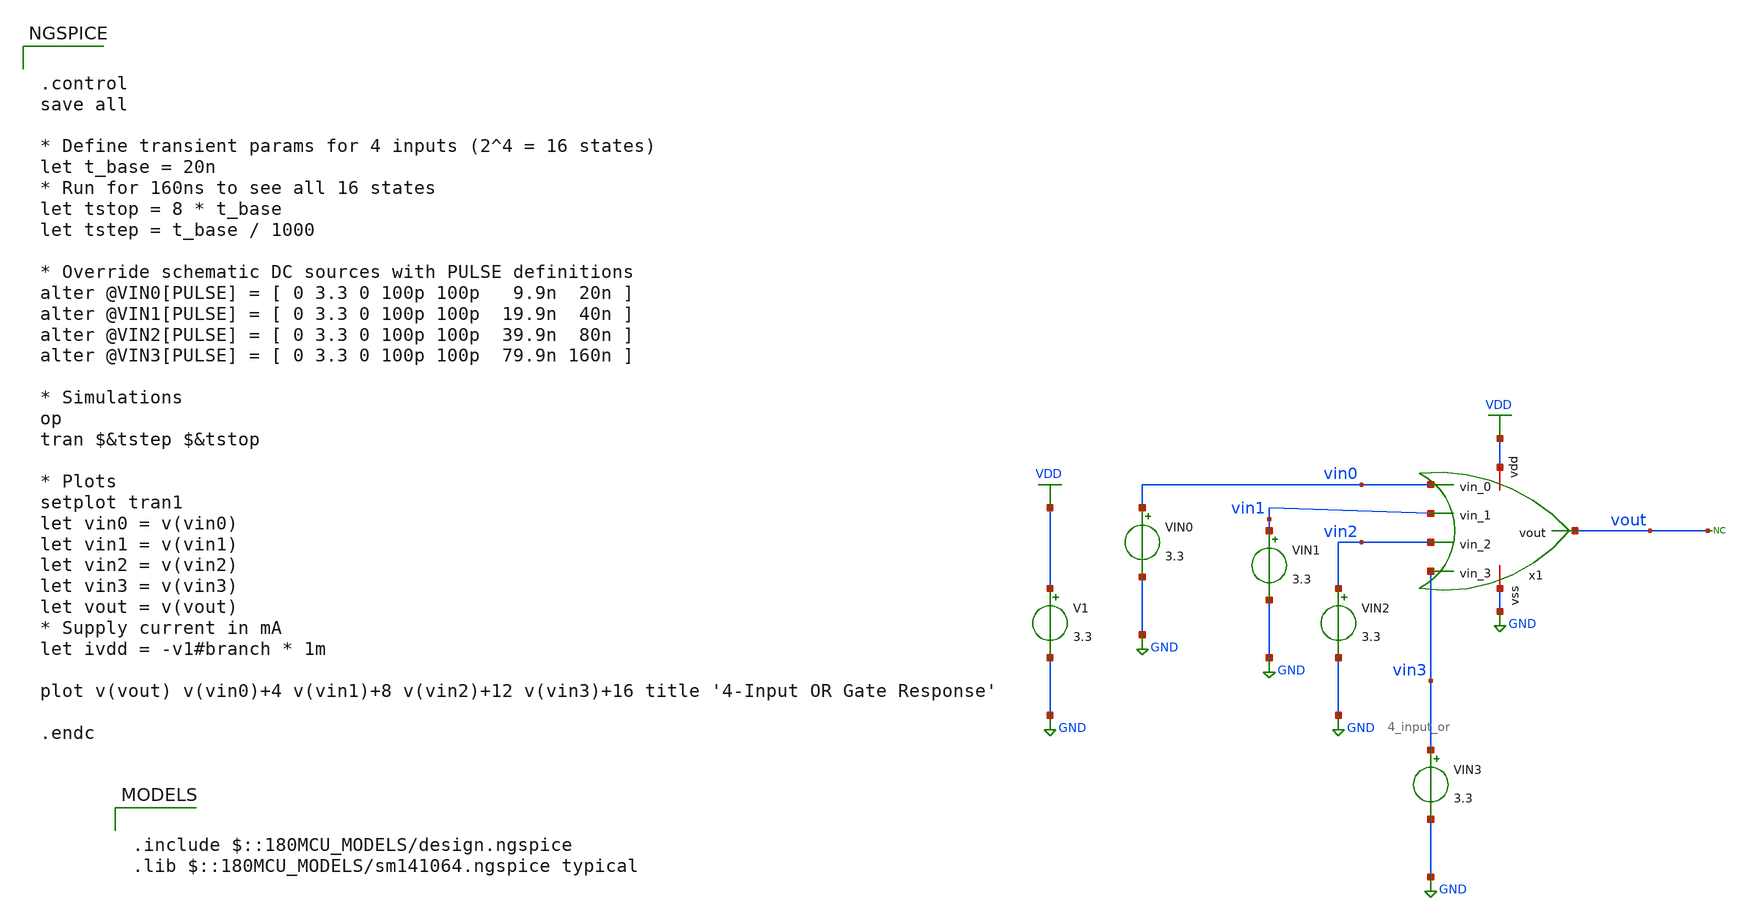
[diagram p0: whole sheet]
** sch_path: designs/4_input_or_tb.sch
**.subckt 4_input_or_tb
V1 VDD GND 3.3
VIN0 vin0 GND 3.3
* noconn vout
VIN2 vin2 GND 3.3
VIN1 vin1 GND 3.3
x1 VDD vin0 vin1 vin2 vin3 vout GND 4_input_or
VIN3 vin3 GND 3.3
**** begin user architecture code

.include $::180MCU_MODELS/design.ngspice
.lib $::180MCU_MODELS/sm141064.ngspice typical



.control
save all

* Define transient params for 4 inputs (2^4 = 16 states)
let t_base = 20n
* Run for 160ns to see all 16 states
let tstop = 8 * t_base
let tstep = t_base / 1000

* Override schematic DC sources with PULSE definitions
alter @VIN0[PULSE] = [ 0 3.3 0 100p 100p   9.9n  20n ]
alter @VIN1[PULSE] = [ 0 3.3 0 100p 100p  19.9n  40n ]
alter @VIN2[PULSE] = [ 0 3.3 0 100p 100p  39.9n  80n ]
alter @VIN3[PULSE] = [ 0 3.3 0 100p 100p  79.9n 160n ]

* Simulations
op
tran $&tstep $&tstop

* Plots
setplot tran1
let vin0 = v(vin0)
let vin1 = v(vin1)
let vin2 = v(vin2)
let vin3 = v(vin3)
let vout = v(vout)
* Supply current in mA
let ivdd = -v1#branch * 1m

plot v(vout) v(vin0)+4 v(vin1)+8 v(vin2)+12 v(vin3)+16 title '4-Input OR Gate Response'

.endc


**** end user architecture code
**.ends

* expanding   symbol:  4_input_or.sym # of pins=7
** sym_path: designs/4_input_or.sym
** sch_path: designs/4_input_or.sch
.subckt 4_input_or vdd vin_0 vin_1 vin_2 vin_3 vout vss
*.iopin vdd
*.iopin vss
*.ipin vin_0
*.ipin vin_1
*.ipin vin_2
*.ipin vin_3
*.opin vout
XM1 net1 vin_0 vdd vdd pfet_03v3 L=0.28u W=0.22u nf=1 ad='int((nf+1)/2) * W/nf * 0.18u' as='int((nf+2)/2) * W/nf * 0.18u'
+ pd='2*int((nf+1)/2) * (W/nf + 0.18u)' ps='2*int((nf+2)/2) * (W/nf + 0.18u)' nrd='0.18u / W' nrs='0.18u / W'
+ sa=0 sb=0 sd=0 m=1
XM2 net4 vin_3 vss vss nfet_03v3 L=0.28u W=0.22u nf=1 ad='int((nf+1)/2) * W/nf * 0.18u' as='int((nf+2)/2) * W/nf * 0.18u'
+ pd='2*int((nf+1)/2) * (W/nf + 0.18u)' ps='2*int((nf+2)/2) * (W/nf + 0.18u)' nrd='0.18u / W' nrs='0.18u / W'
+ sa=0 sb=0 sd=0 m=1
XM3 net2 vin_1 net1 vdd pfet_03v3 L=0.28u W=0.22u nf=1 ad='int((nf+1)/2) * W/nf * 0.18u' as='int((nf+2)/2) * W/nf * 0.18u'
+ pd='2*int((nf+1)/2) * (W/nf + 0.18u)' ps='2*int((nf+2)/2) * (W/nf + 0.18u)' nrd='0.18u / W' nrs='0.18u / W'
+ sa=0 sb=0 sd=0 m=1
XM4 net3 vin_2 net2 vdd pfet_03v3 L=0.28u W=0.22u nf=1 ad='int((nf+1)/2) * W/nf * 0.18u' as='int((nf+2)/2) * W/nf * 0.18u'
+ pd='2*int((nf+1)/2) * (W/nf + 0.18u)' ps='2*int((nf+2)/2) * (W/nf + 0.18u)' nrd='0.18u / W' nrs='0.18u / W'
+ sa=0 sb=0 sd=0 m=1
XM5 net4 vin_3 net3 vdd pfet_03v3 L=0.28u W=0.22u nf=1 ad='int((nf+1)/2) * W/nf * 0.18u' as='int((nf+2)/2) * W/nf * 0.18u'
+ pd='2*int((nf+1)/2) * (W/nf + 0.18u)' ps='2*int((nf+2)/2) * (W/nf + 0.18u)' nrd='0.18u / W' nrs='0.18u / W'
+ sa=0 sb=0 sd=0 m=1
XM6 net4 vin_2 vss vss nfet_03v3 L=0.28u W=0.22u nf=1 ad='int((nf+1)/2) * W/nf * 0.18u' as='int((nf+2)/2) * W/nf * 0.18u'
+ pd='2*int((nf+1)/2) * (W/nf + 0.18u)' ps='2*int((nf+2)/2) * (W/nf + 0.18u)' nrd='0.18u / W' nrs='0.18u / W'
+ sa=0 sb=0 sd=0 m=1
XM7 net4 vin_1 vss vss nfet_03v3 L=0.28u W=0.22u nf=1 ad='int((nf+1)/2) * W/nf * 0.18u' as='int((nf+2)/2) * W/nf * 0.18u'
+ pd='2*int((nf+1)/2) * (W/nf + 0.18u)' ps='2*int((nf+2)/2) * (W/nf + 0.18u)' nrd='0.18u / W' nrs='0.18u / W'
+ sa=0 sb=0 sd=0 m=1
XM8 net4 vin_0 vss vss nfet_03v3 L=0.28u W=0.22u nf=1 ad='int((nf+1)/2) * W/nf * 0.18u' as='int((nf+2)/2) * W/nf * 0.18u'
+ pd='2*int((nf+1)/2) * (W/nf + 0.18u)' ps='2*int((nf+2)/2) * (W/nf + 0.18u)' nrd='0.18u / W' nrs='0.18u / W'
+ sa=0 sb=0 sd=0 m=1
XM9 vout net4 vdd vdd pfet_03v3 L=0.28u W=0.22u nf=1 ad='int((nf+1)/2) * W/nf * 0.18u' as='int((nf+2)/2) * W/nf * 0.18u'
+ pd='2*int((nf+1)/2) * (W/nf + 0.18u)' ps='2*int((nf+2)/2) * (W/nf + 0.18u)' nrd='0.18u / W' nrs='0.18u / W'
+ sa=0 sb=0 sd=0 m=1
XM10 vout net4 vss vss nfet_03v3 L=0.28u W=0.22u nf=1 ad='int((nf+1)/2) * W/nf * 0.18u' as='int((nf+2)/2) * W/nf * 0.18u'
+ pd='2*int((nf+1)/2) * (W/nf + 0.18u)' ps='2*int((nf+2)/2) * (W/nf + 0.18u)' nrd='0.18u / W' nrs='0.18u / W'
+ sa=0 sb=0 sd=0 m=1
.ends

.GLOBAL VDD
.GLOBAL GND
.end
